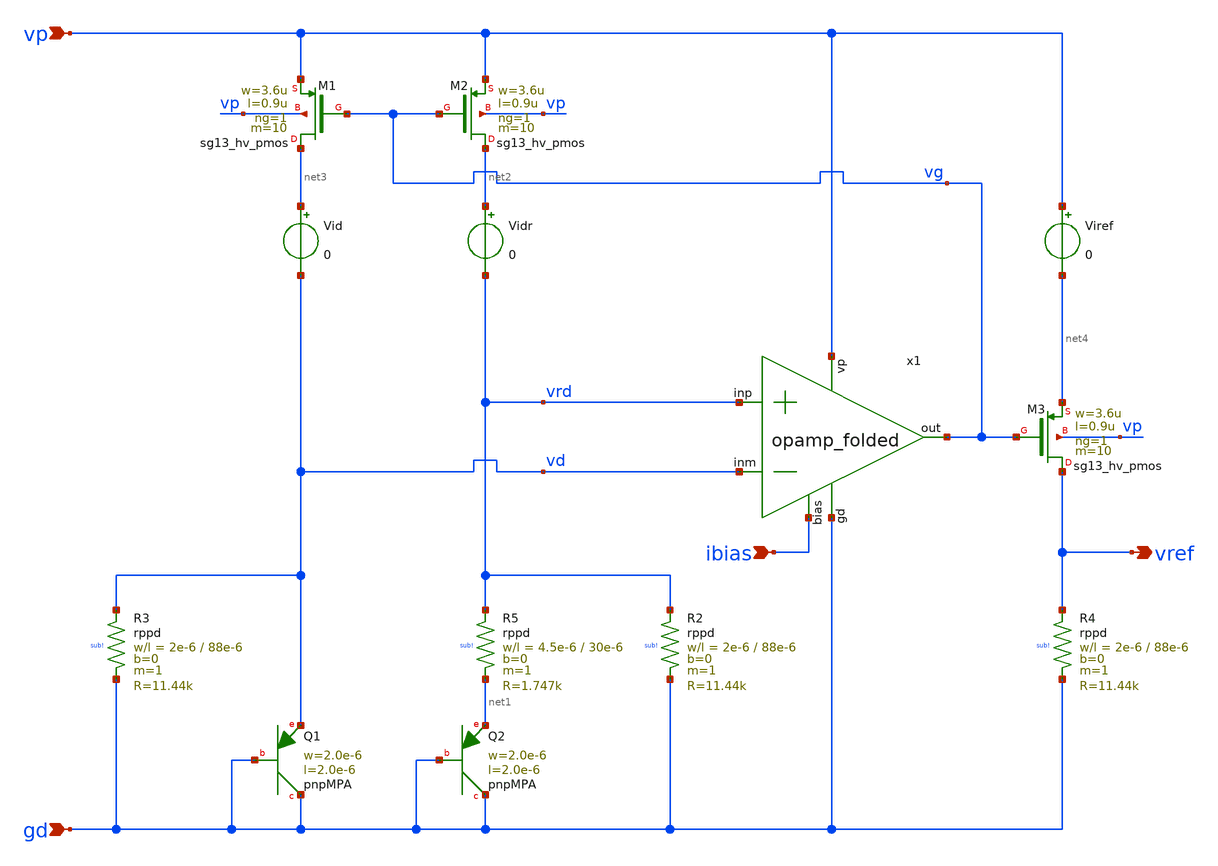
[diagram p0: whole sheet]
** sch_path: bandgap_res/bandgap_res.sch
**.subckt bandgap_res gd vp ibias vref
*.ipin gd
*.ipin vp
*.ipin ibias
*.opin vref
XQ1 gd gd vd pnpMPA a=4p p=8u m=1
XQ2 gd gd net1 pnpMPA a=4p p=8u m=8
x1 vp vrd vd vg ibias gd opamp_folded
XM2 net2 vg vp vp sg13_hv_pmos w=3.6u l=0.9u ng=1 m=10 mm_ok=1
XM1 net3 vg vp vp sg13_hv_pmos w=3.6u l=0.9u ng=1 m=10 mm_ok=1
Vid net3 vd 0
.save i(vid)
Vidr net2 vrd 0
.save i(vidr)
Viref vp net4 0
.save i(viref)
XM3 vref vg net4 vp sg13_hv_pmos w=3.6u l=0.9u ng=1 m=10 mm_ok=1
XR2 vrd gd sub! rppd w=2e-6 l=88e-6 m=1 b=0 mm_ok=1
XR3 vd gd sub! rppd w=2e-6 l=88e-6 m=1 b=0 mm_ok=1
XR4 vref gd sub! rppd w=2e-6 l=88e-6 m=1 b=0 mm_ok=1
XR5 vrd net1 sub! rppd w=4.5e-6 l=30e-6 m=1 b=0 mm_ok=1
**.ends

* expanding   symbol:  /foss/designs/master/bandgap_res/opamp_folded.sym # of pins=6
** sym_path: /foss/designs/master/bandgap_res/opamp_folded.sym
** sch_path: /foss/designs/master/bandgap_res/opamp_folded.sch
.subckt opamp_folded vp inp inm out bias gd
*.ipin bias
*.opin out
*.ipin vp
*.ipin inp
*.ipin inm
*.ipin gd
XM1 inp_fold inp net1 gd sg13_hv_nmos w=1.2u l=0.9u ng=1 m=6 mm_ok=1
XM2 inm_fold inm net1 gd sg13_hv_nmos w=1.2u l=0.9u ng=1 m=6 mm_ok=1
XM3 tele_p tele_g gd gd sg13_hv_nmos w=1.2u l=0.9u ng=1 m=2 mm_ok=1
XM4 tele_m tele_g gd gd sg13_hv_nmos w=1.2u l=0.9u ng=1 m=2 mm_ok=1
XM5 tele_g bias2 tele_p gd sg13_hv_nmos w=1.2u l=0.9u ng=1 m=2 mm_ok=1
XM6 out bias2 tele_m gd sg13_hv_nmos w=1.2u l=0.9u ng=1 m=2 mm_ok=1
XM7 tele_g bias3 inp_fold vp sg13_hv_pmos w=3.6u l=0.9u ng=1 m=2 mm_ok=1
XM8 out bias3 inm_fold vp sg13_hv_pmos w=3.6u l=0.9u ng=1 m=2 mm_ok=1
XM9 inp_fold bias4 vp vp sg13_hv_pmos w=3.6u l=0.9u ng=1 m=4 mm_ok=1
XM10 inm_fold bias4 vp vp sg13_hv_pmos w=3.6u l=0.9u ng=1 m=4 mm_ok=1
XM11 net1 bias gd gd sg13_hv_nmos w=1.2u l=0.9u ng=1 m=4 mm_ok=1
XM12 bias bias gd gd sg13_hv_nmos w=1.2u l=0.9u ng=1 m=2 mm_ok=1
XM13 bias4 bias gd gd sg13_hv_nmos w=1.2u l=0.9u ng=1 m=2 mm_ok=1
XM14 bias4 bias4 vp vp sg13_hv_pmos w=3.6u l=0.9u ng=1 m=2 mm_ok=1
XM15 bias3 bias gd gd sg13_hv_nmos w=1.2u l=0.9u ng=1 m=2 mm_ok=1
XM16 bias3 bias3 net3 vp sg13_hv_pmos w=3.6u l=0.9u ng=1 m=1 mm_ok=1
XM17 net3 bias3 vp vp sg13_hv_pmos w=3.6u l=0.9u ng=1 m=1 mm_ok=1
XM18 net2 bias2 gd gd sg13_hv_nmos w=1.2u l=0.9u ng=1 m=1 mm_ok=1
XM19 bias2 bias2 net2 gd sg13_hv_nmos w=1.2u l=0.9u ng=1 m=1 mm_ok=1
XM20 bias2 bias4 vp vp sg13_hv_pmos w=3.6u l=0.9u ng=1 m=4 mm_ok=1
XM21 gd bias gd gd sg13_hv_nmos w=1.2u l=0.9u ng=1 m=8 mm_ok=1
.ends

.end
